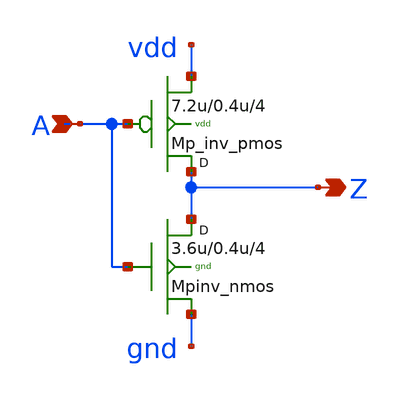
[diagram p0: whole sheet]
** sch_path: sram_4_16_scn4m/pinv_8.sch
**.subckt pinv_8 A Z
*.ipin A
*.opin Z
Mpinv_nmos Z A gnd gnd n w=3.6u l=0.4u m=4
Mp_inv_pmos Z A vdd vdd p w=7.2u l=0.4u m=4
**.ends
.end
